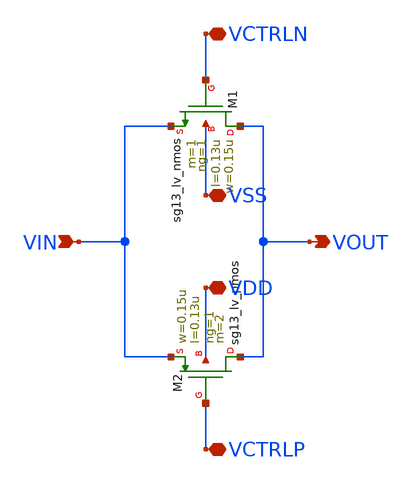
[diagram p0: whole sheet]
** sch_path: ADC8711-main/schematic/xschem/TG_2C.sch
**.subckt TG_2C VCTRLN VCTRLP VOUT VIN VSS VDD
*.iopin VCTRLN
*.iopin VCTRLP
*.opin VOUT
*.ipin VIN
*.iopin VSS
*.iopin VDD
XM1 VOUT VCTRLN VIN VSS sg13_lv_nmos w=0.15u l=0.13u ng=1 m=1 mm_ok=1
XM2 VOUT VCTRLP VIN VDD sg13_lv_pmos w=0.15u l=0.13u ng=1 m=2 mm_ok=1
**.ends
.end
